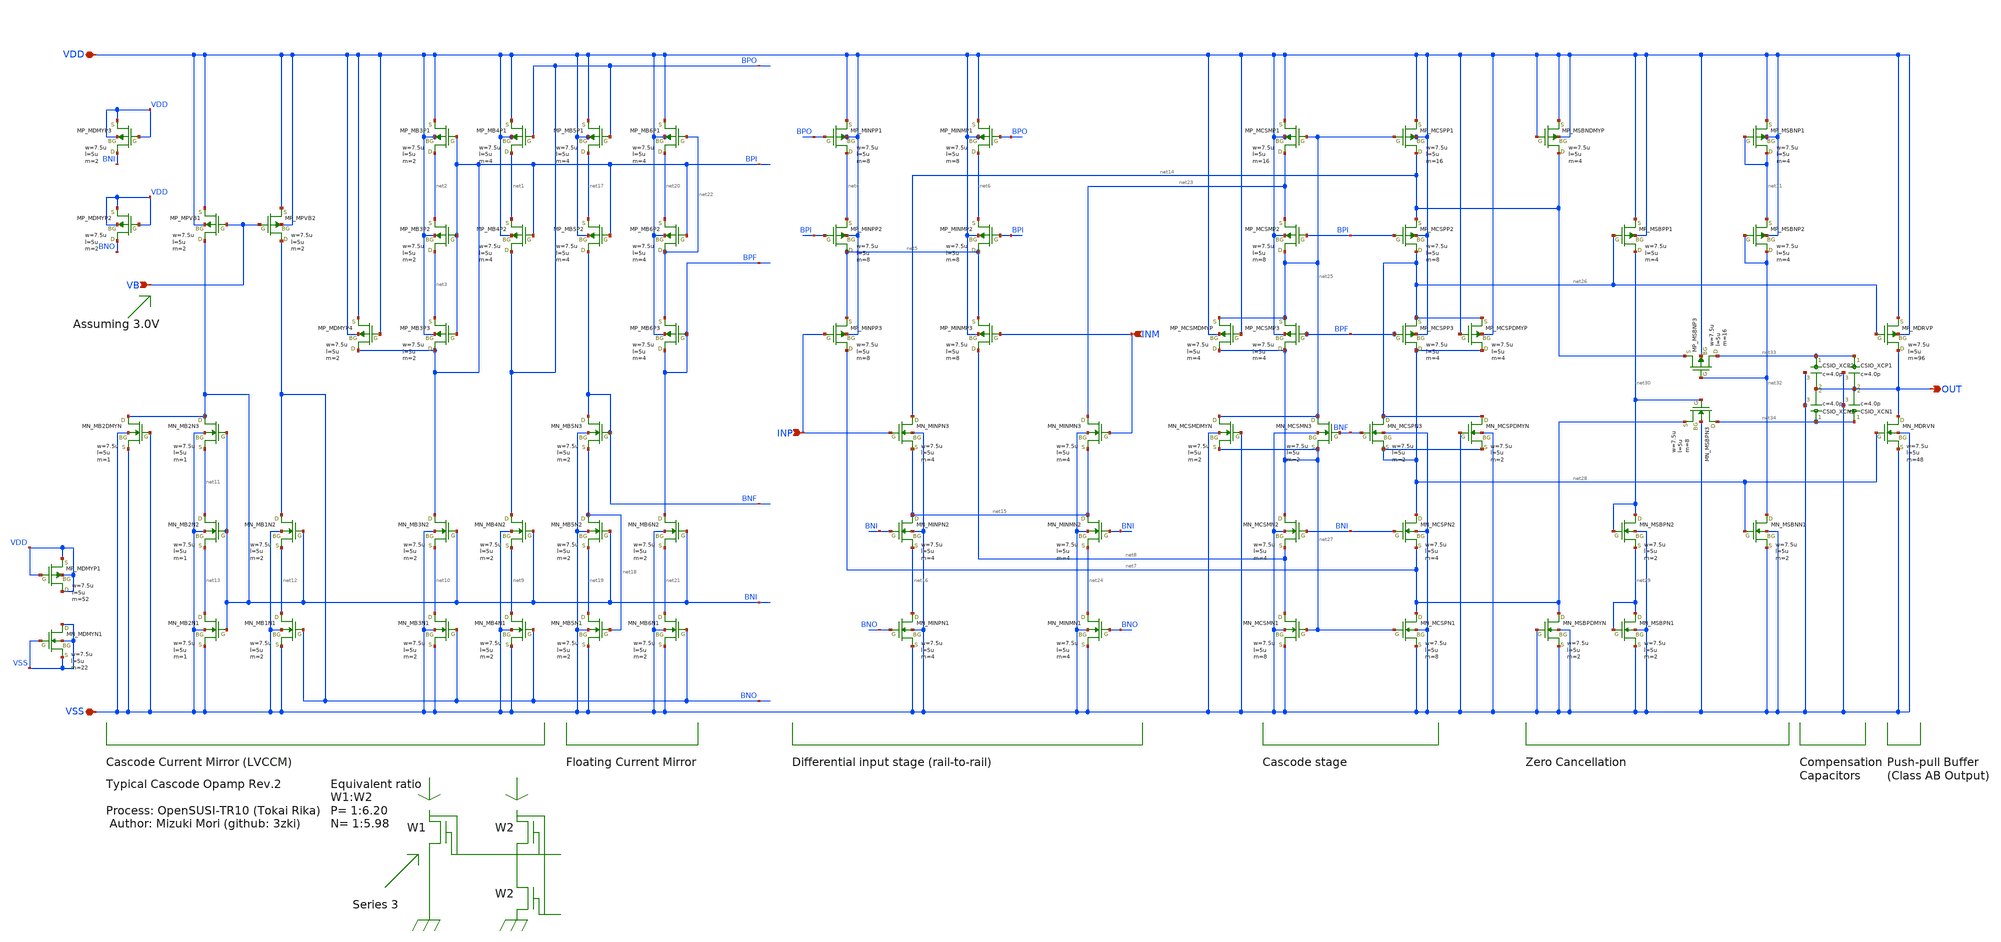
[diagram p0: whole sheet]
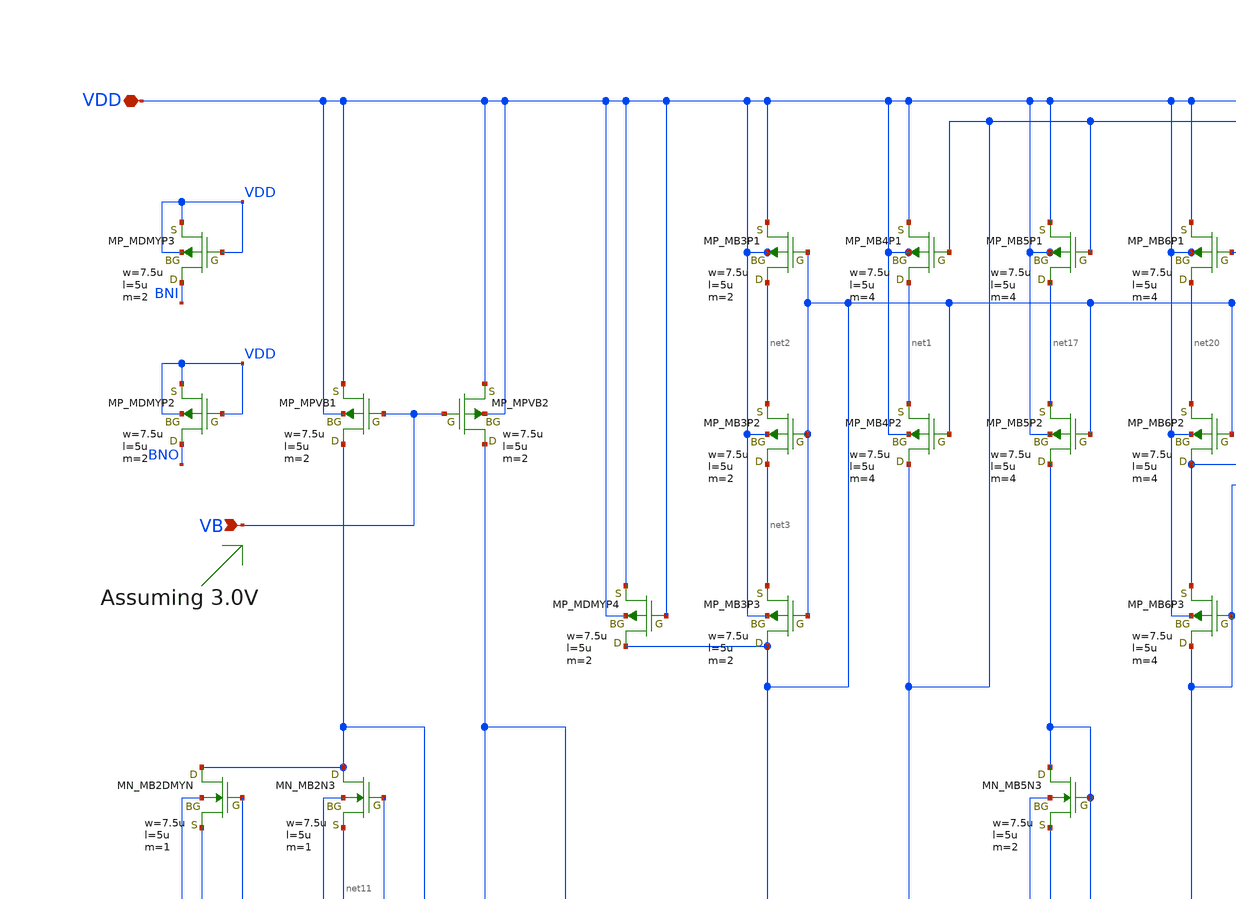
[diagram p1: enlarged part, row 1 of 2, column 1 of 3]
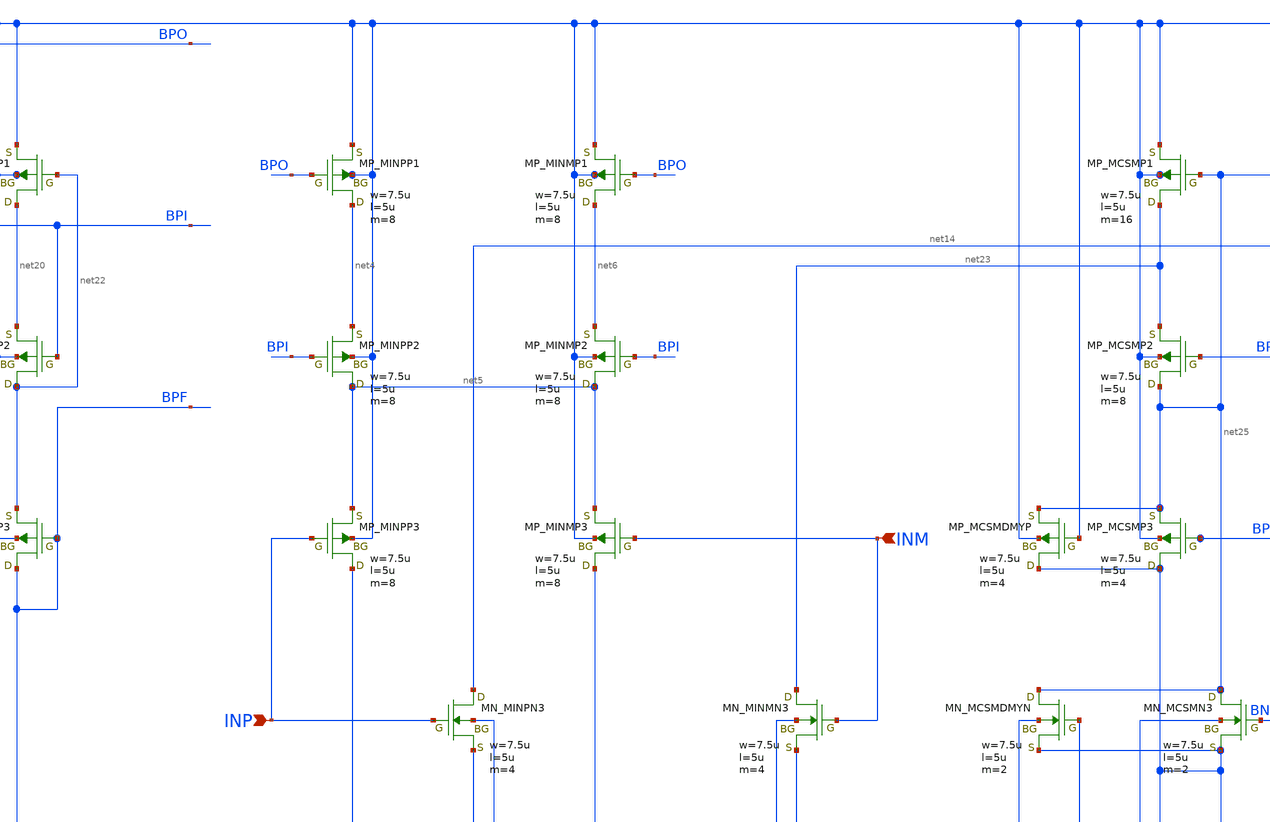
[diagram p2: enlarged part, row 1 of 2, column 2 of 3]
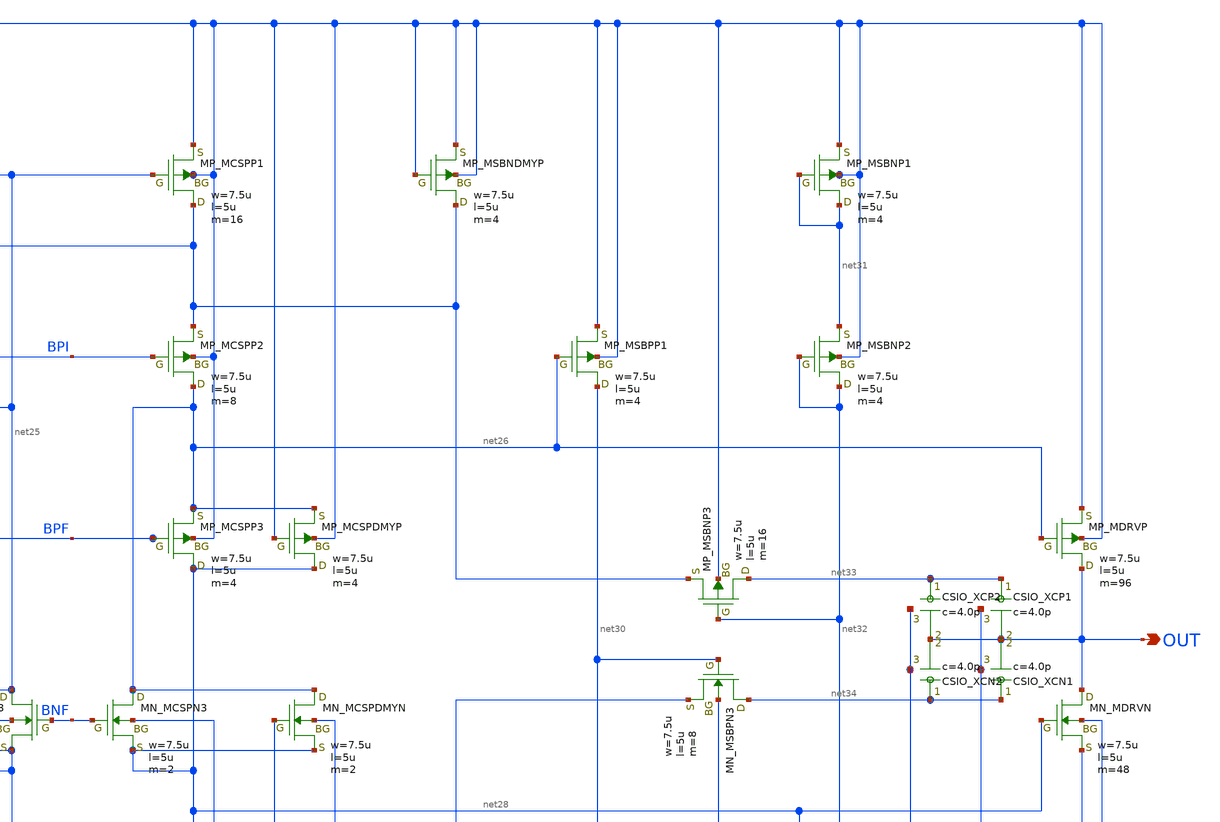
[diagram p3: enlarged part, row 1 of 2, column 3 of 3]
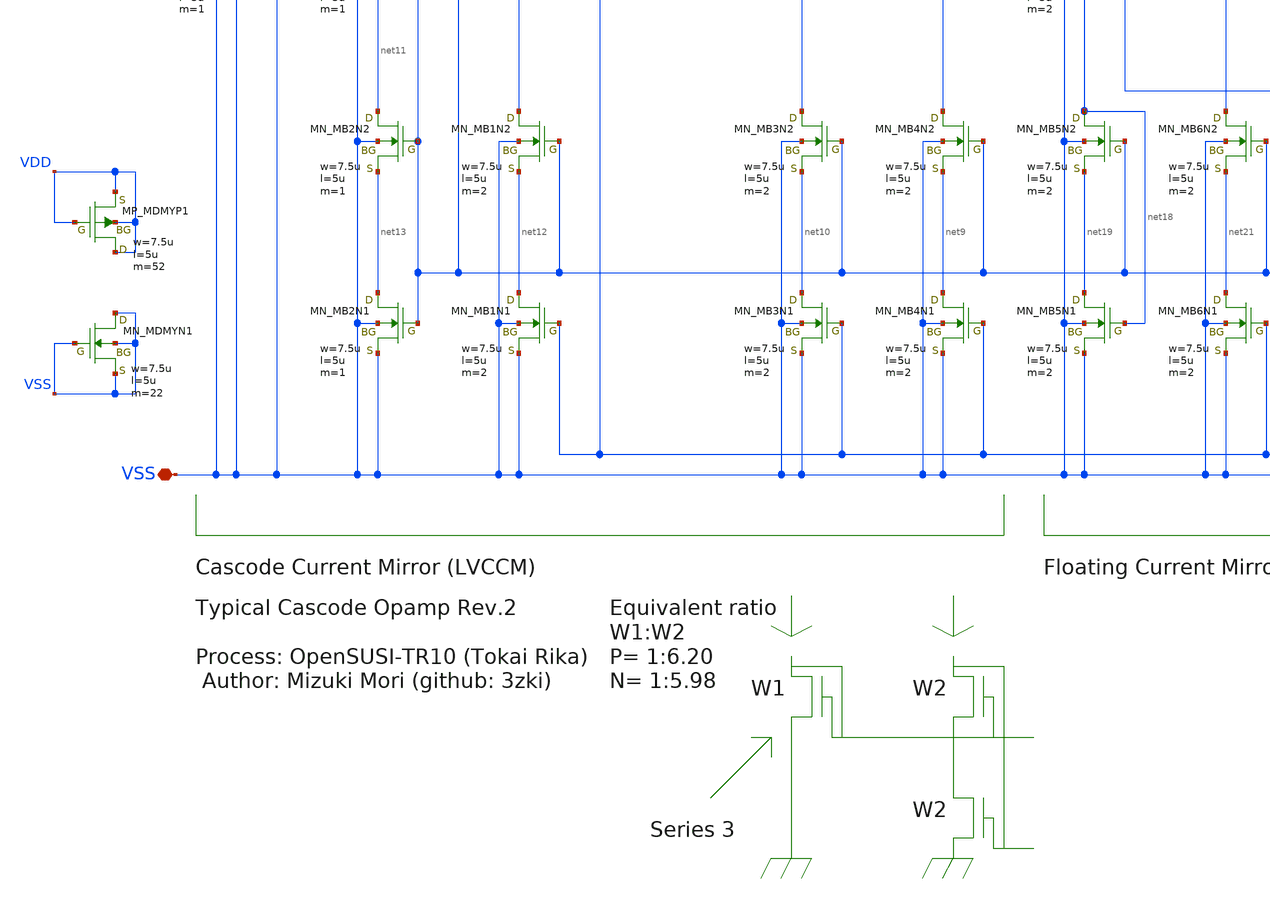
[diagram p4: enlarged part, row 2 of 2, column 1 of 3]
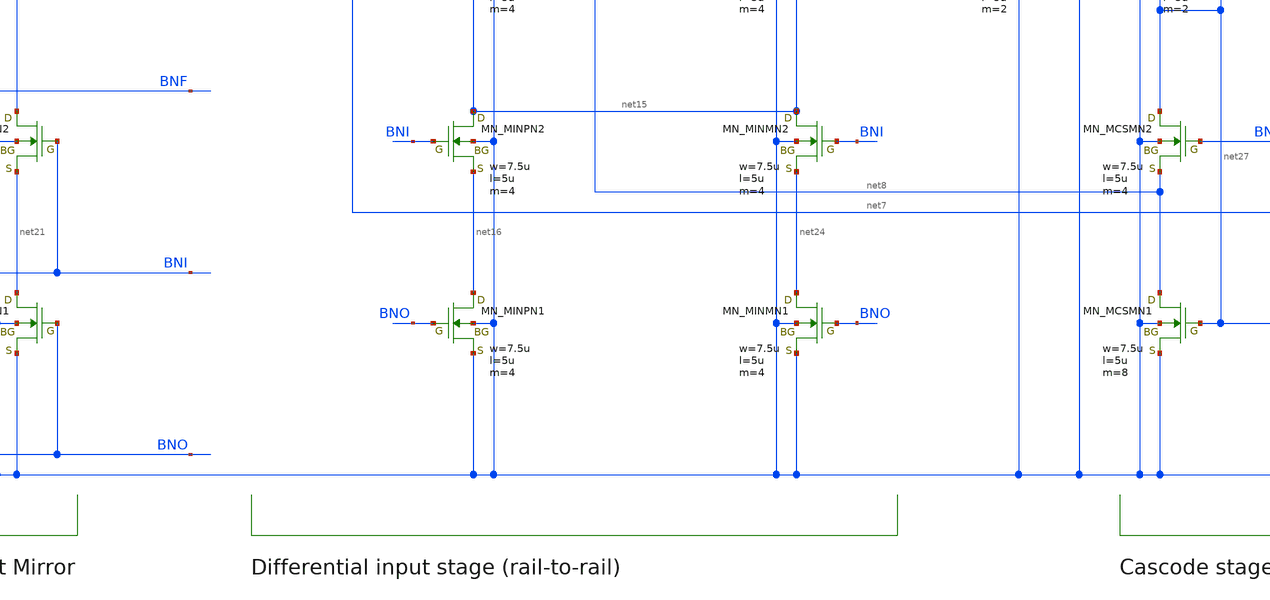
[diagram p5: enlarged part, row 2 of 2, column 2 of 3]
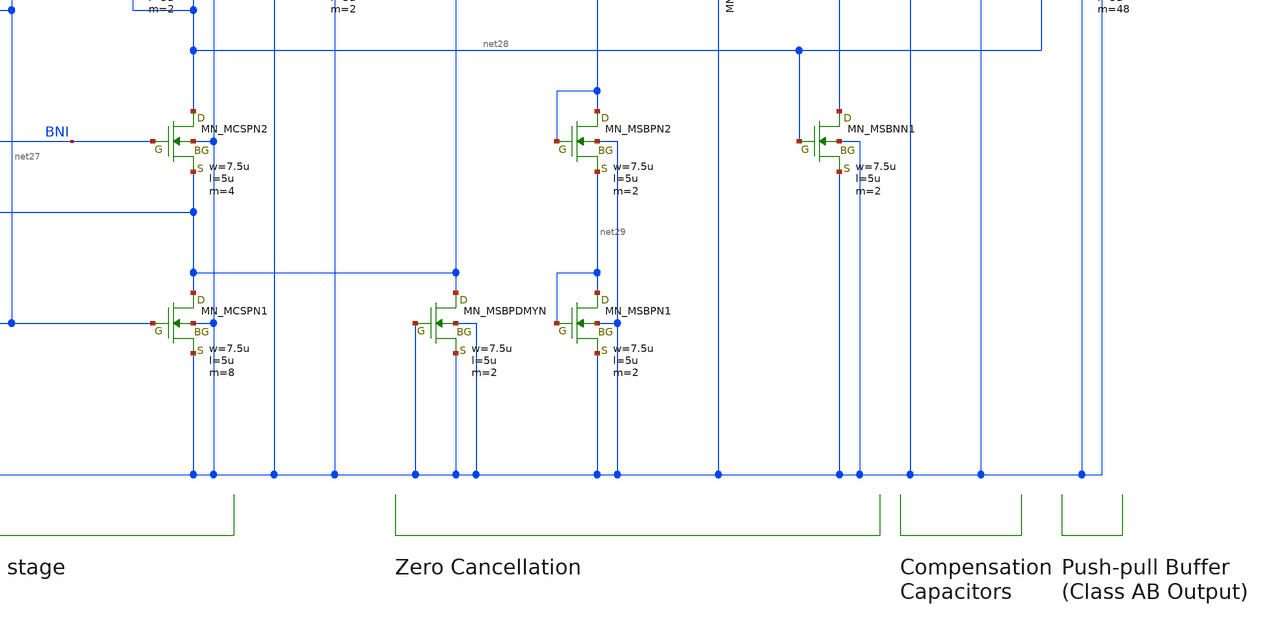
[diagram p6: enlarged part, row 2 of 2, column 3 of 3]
** sch_path: OpenSUSI-TR10/opamp_r2r_audio/opamp_r2r_allinone.sch
**.subckt opamp_r2r_allinone VDD VSS INP INM OUT VB
*.iopin VDD
*.iopin VSS
*.ipin INP
*.ipin INM
*.opin OUT
*.ipin VB
XMDRVP OUT net26 VDD VDD PMOS w=7.5u l=5u as=0 ad=0 ps=0 pd=0 nrd=0 nrs=0 m=96
XMDRVN OUT net28 VSS VSS NMOS w=7.5u l=5u as=0 ad=0 ps=0 pd=0 nrd=0 nrs=0 m=48
XMB4P1 net1 BPO VDD VDD PMOS w=7.5u l=5u as=0 ad=0 ps=0 pd=0 nrd=0 nrs=0 m=4
XMB4P2 BPO BPI net1 VDD PMOS w=7.5u l=5u as=0 ad=0 ps=0 pd=0 nrd=0 nrs=0 m=4
XMB3P1 net2 BPI VDD VDD PMOS w=7.5u l=5u as=0 ad=0 ps=0 pd=0 nrd=0 nrs=0 m=2
XMB3P2 net3 BPI net2 VDD PMOS w=7.5u l=5u as=0 ad=0 ps=0 pd=0 nrd=0 nrs=0 m=2
XMB3P3 BPI BPI net3 VDD PMOS w=7.5u l=5u as=0 ad=0 ps=0 pd=0 nrd=0 nrs=0 m=2
XMINPP1 net4 BPO VDD VDD PMOS w=7.5u l=5u as=0 ad=0 ps=0 pd=0 nrd=0 nrs=0 m=8
XMINPP2 net5 BPI net4 VDD PMOS w=7.5u l=5u as=0 ad=0 ps=0 pd=0 nrd=0 nrs=0 m=8
XMINPP3 net7 INP net5 VDD PMOS w=7.5u l=5u as=0 ad=0 ps=0 pd=0 nrd=0 nrs=0 m=8
XMINMP1 net6 BPO VDD VDD PMOS w=7.5u l=5u as=0 ad=0 ps=0 pd=0 nrd=0 nrs=0 m=8
XMINMP2 net5 BPI net6 VDD PMOS w=7.5u l=5u as=0 ad=0 ps=0 pd=0 nrd=0 nrs=0 m=8
XMINMP3 net8 INM net5 VDD PMOS w=7.5u l=5u as=0 ad=0 ps=0 pd=0 nrd=0 nrs=0 m=8
XMB4N2 BPO BNI net9 VSS NMOS w=7.5u l=5u as=0 ad=0 ps=0 pd=0 nrd=0 nrs=0 m=2
XMB3N2 BPI BNI net10 VSS NMOS w=7.5u l=5u as=0 ad=0 ps=0 pd=0 nrd=0 nrs=0 m=2
XMB4N1 net9 BNO VSS VSS NMOS w=7.5u l=5u as=0 ad=0 ps=0 pd=0 nrd=0 nrs=0 m=2
XMB3N1 net10 BNO VSS VSS NMOS w=7.5u l=5u as=0 ad=0 ps=0 pd=0 nrd=0 nrs=0 m=2
XMB1N2 BNO BNI net12 VSS NMOS w=7.5u l=5u as=0 ad=0 ps=0 pd=0 nrd=0 nrs=0 m=2
XMB2N2 net11 BNI net13 VSS NMOS w=7.5u l=5u as=0 ad=0 ps=0 pd=0 nrd=0 nrs=0 m=1
XMB1N1 net12 BNO VSS VSS NMOS w=7.5u l=5u as=0 ad=0 ps=0 pd=0 nrd=0 nrs=0 m=2
XMB2N1 net13 BNI VSS VSS NMOS w=7.5u l=5u as=0 ad=0 ps=0 pd=0 nrd=0 nrs=0 m=1
XMB2N3 BNI BNI net11 VSS NMOS w=7.5u l=5u as=0 ad=0 ps=0 pd=0 nrd=0 nrs=0 m=1
XMINPN2 net15 BNI net16 VSS NMOS w=7.5u l=5u as=0 ad=0 ps=0 pd=0 nrd=0 nrs=0 m=4
XMINPN1 net16 BNO VSS VSS NMOS w=7.5u l=5u as=0 ad=0 ps=0 pd=0 nrd=0 nrs=0 m=4
XMINPN3 net14 INP net15 VSS NMOS w=7.5u l=5u as=0 ad=0 ps=0 pd=0 nrd=0 nrs=0 m=4
XMB5P1 net17 BPO VDD VDD PMOS w=7.5u l=5u as=0 ad=0 ps=0 pd=0 nrd=0 nrs=0 m=4
XMB5P2 BNF BPI net17 VDD PMOS w=7.5u l=5u as=0 ad=0 ps=0 pd=0 nrd=0 nrs=0 m=4
XMB5N2 net18 BNI net19 VSS NMOS w=7.5u l=5u as=0 ad=0 ps=0 pd=0 nrd=0 nrs=0 m=2
XMB5N1 net19 net18 VSS VSS NMOS w=7.5u l=5u as=0 ad=0 ps=0 pd=0 nrd=0 nrs=0 m=2
XMB5N3 BNF BNF net18 VSS NMOS w=7.5u l=5u as=0 ad=0 ps=0 pd=0 nrd=0 nrs=0 m=2
XMB6P1 net20 net22 VDD VDD PMOS w=7.5u l=5u as=0 ad=0 ps=0 pd=0 nrd=0 nrs=0 m=4
XMB6P2 net22 BPI net20 VDD PMOS w=7.5u l=5u as=0 ad=0 ps=0 pd=0 nrd=0 nrs=0 m=4
XMB6N2 BPF BNI net21 VSS NMOS w=7.5u l=5u as=0 ad=0 ps=0 pd=0 nrd=0 nrs=0 m=2
XMB6N1 net21 BNO VSS VSS NMOS w=7.5u l=5u as=0 ad=0 ps=0 pd=0 nrd=0 nrs=0 m=2
XMB6P3 BPF BPF net22 VDD PMOS w=7.5u l=5u as=0 ad=0 ps=0 pd=0 nrd=0 nrs=0 m=4
XMB2DMYN BNI VSS VSS VSS NMOS w=7.5u l=5u as=0 ad=0 ps=0 pd=0 nrd=0 nrs=0 m=1
XMINMN2 net15 BNI net24 VSS NMOS w=7.5u l=5u as=0 ad=0 ps=0 pd=0 nrd=0 nrs=0 m=4
XMINMN1 net24 BNO VSS VSS NMOS w=7.5u l=5u as=0 ad=0 ps=0 pd=0 nrd=0 nrs=0 m=4
XMINMN3 net23 INM net15 VSS NMOS w=7.5u l=5u as=0 ad=0 ps=0 pd=0 nrd=0 nrs=0 m=4
XMCSMP1 net23 net25 VDD VDD PMOS w=7.5u l=5u as=0 ad=0 ps=0 pd=0 nrd=0 nrs=0 m=16
XMCSMP2 net25 BPI net23 VDD PMOS w=7.5u l=5u as=0 ad=0 ps=0 pd=0 nrd=0 nrs=0 m=8
XMCSMP3 net27 BPF net25 VDD PMOS w=7.5u l=5u as=0 ad=0 ps=0 pd=0 nrd=0 nrs=0 m=4
XMCSPP1 net14 net25 VDD VDD PMOS w=7.5u l=5u as=0 ad=0 ps=0 pd=0 nrd=0 nrs=0 m=16
XMCSPP2 net26 BPI net14 VDD PMOS w=7.5u l=5u as=0 ad=0 ps=0 pd=0 nrd=0 nrs=0 m=8
XMCSPP3 net28 BPF net26 VDD PMOS w=7.5u l=5u as=0 ad=0 ps=0 pd=0 nrd=0 nrs=0 m=4
XMCSMN2 net27 BNI net8 VSS NMOS w=7.5u l=5u as=0 ad=0 ps=0 pd=0 nrd=0 nrs=0 m=4
XMCSMN1 net8 net27 VSS VSS NMOS w=7.5u l=5u as=0 ad=0 ps=0 pd=0 nrd=0 nrs=0 m=8
XMCSMN3 net25 BNF net27 VSS NMOS w=7.5u l=5u as=0 ad=0 ps=0 pd=0 nrd=0 nrs=0 m=2
XMCSPN3 net26 BNF net28 VSS NMOS w=7.5u l=5u as=0 ad=0 ps=0 pd=0 nrd=0 nrs=0 m=2
XMCSPN2 net28 BNI net7 VSS NMOS w=7.5u l=5u as=0 ad=0 ps=0 pd=0 nrd=0 nrs=0 m=4
XMCSPN1 net7 net27 VSS VSS NMOS w=7.5u l=5u as=0 ad=0 ps=0 pd=0 nrd=0 nrs=0 m=8
XMSBPN2 net30 net30 net29 VSS NMOS w=7.5u l=5u as=0 ad=0 ps=0 pd=0 nrd=0 nrs=0 m=2
XMSBPN1 net29 net29 VSS VSS NMOS w=7.5u l=5u as=0 ad=0 ps=0 pd=0 nrd=0 nrs=0 m=2
XMSBPP1 net30 net26 VDD VDD PMOS w=7.5u l=5u as=0 ad=0 ps=0 pd=0 nrd=0 nrs=0 m=4
XMSBNP1 net31 net31 VDD VDD PMOS w=7.5u l=5u as=0 ad=0 ps=0 pd=0 nrd=0 nrs=0 m=4
XMSBNP2 net32 net32 net31 VDD PMOS w=7.5u l=5u as=0 ad=0 ps=0 pd=0 nrd=0 nrs=0 m=4
XMSBNN1 net32 net28 VSS VSS NMOS w=7.5u l=5u as=0 ad=0 ps=0 pd=0 nrd=0 nrs=0 m=2
XMSBNP3 net33 net32 net14 VDD PMOS w=7.5u l=5u as=0 ad=0 ps=0 pd=0 nrd=0 nrs=0 m=16
XMSBPN3 net34 net30 net7 VSS NMOS w=7.5u l=5u as=0 ad=0 ps=0 pd=0 nrd=0 nrs=0 m=8
XMSBPDMYN net7 VSS VSS VSS NMOS w=7.5u l=5u as=0 ad=0 ps=0 pd=0 nrd=0 nrs=0 m=2
XMSBNDMYP net14 VDD VDD VDD PMOS w=7.5u l=5u as=0 ad=0 ps=0 pd=0 nrd=0 nrs=0 m=4
XMDMYN1 VSS VSS VSS VSS NMOS w=7.5u l=5u as=0 ad=0 ps=0 pd=0 nrd=0 nrs=0 m=22
XMDMYP1 VDD VDD VDD VDD PMOS w=7.5u l=5u as=0 ad=0 ps=0 pd=0 nrd=0 nrs=0 m=52
XMPVB1 BNI VB VDD VDD PMOS w=7.5u l=5u as=0 ad=0 ps=0 pd=0 nrd=0 nrs=0 m=2
XMPVB2 BNO VB VDD VDD PMOS w=7.5u l=5u as=0 ad=0 ps=0 pd=0 nrd=0 nrs=0 m=2
XMDMYP2 BNO VDD VDD VDD PMOS w=7.5u l=5u as=0 ad=0 ps=0 pd=0 nrd=0 nrs=0 m=2
XMDMYP3 BNI VDD VDD VDD PMOS w=7.5u l=5u as=0 ad=0 ps=0 pd=0 nrd=0 nrs=0 m=2
XMDMYP4 BPI VDD VDD VDD PMOS w=7.5u l=5u as=0 ad=0 ps=0 pd=0 nrd=0 nrs=0 m=2
XMCSMDMYP net27 VDD net25 VDD PMOS w=7.5u l=5u as=0 ad=0 ps=0 pd=0 nrd=0 nrs=0 m=4
XMCSPDMYP net28 VDD net26 VDD PMOS w=7.5u l=5u as=0 ad=0 ps=0 pd=0 nrd=0 nrs=0 m=4
XMCSMDMYN net25 VSS net27 VSS NMOS w=7.5u l=5u as=0 ad=0 ps=0 pd=0 nrd=0 nrs=0 m=2
XMCSPDMYN net26 VSS net28 VSS NMOS w=7.5u l=5u as=0 ad=0 ps=0 pd=0 nrd=0 nrs=0 m=2
XXCP2 net33 OUT VSS F_CSIO c=4.0p x=80.6u y=80.6u m=1
XXCN2 net34 OUT VSS F_CSIO c=4.0p x=80.6u y=80.6u m=1
XXCP1 net33 OUT VSS F_CSIO c=4.0p x=80.6u y=80.6u m=1
XXCN1 net34 OUT VSS F_CSIO c=4.0p x=80.6u y=80.6u m=1
**.ends
.end
